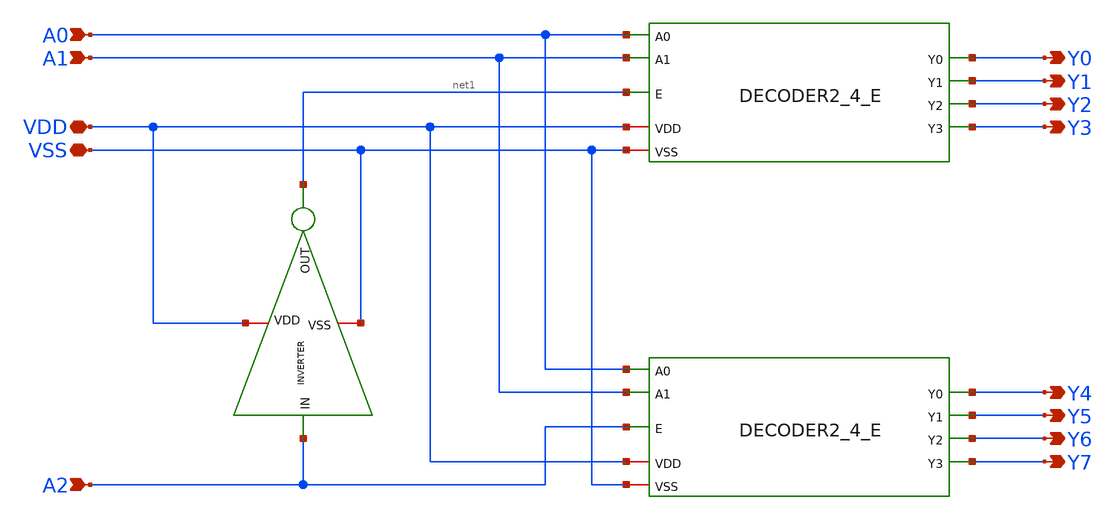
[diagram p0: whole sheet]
** sch_path: DECODER3TO8/Schematic/DECODER3_8.sch
**.subckt DECODER3_8 A0 A1 A2 VDD VSS Y0 Y1 Y2 Y3 Y4 Y5 Y6 Y7
*.ipin A0
*.ipin A1
*.ipin A2
*.iopin VDD
*.iopin VSS
*.opin Y0
*.opin Y1
*.opin Y2
*.opin Y3
*.opin Y4
*.opin Y5
*.opin Y6
*.opin Y7
x1 VDD A0 Y0 A1 Y1 Y2 Y3 VSS net1 DECODER2_4_E
x2 VDD A0 Y4 A1 Y5 Y6 Y7 VSS A2 DECODER2_4_E
x3 VDD A2 net1 VSS INVERTER
**.ends
.end
